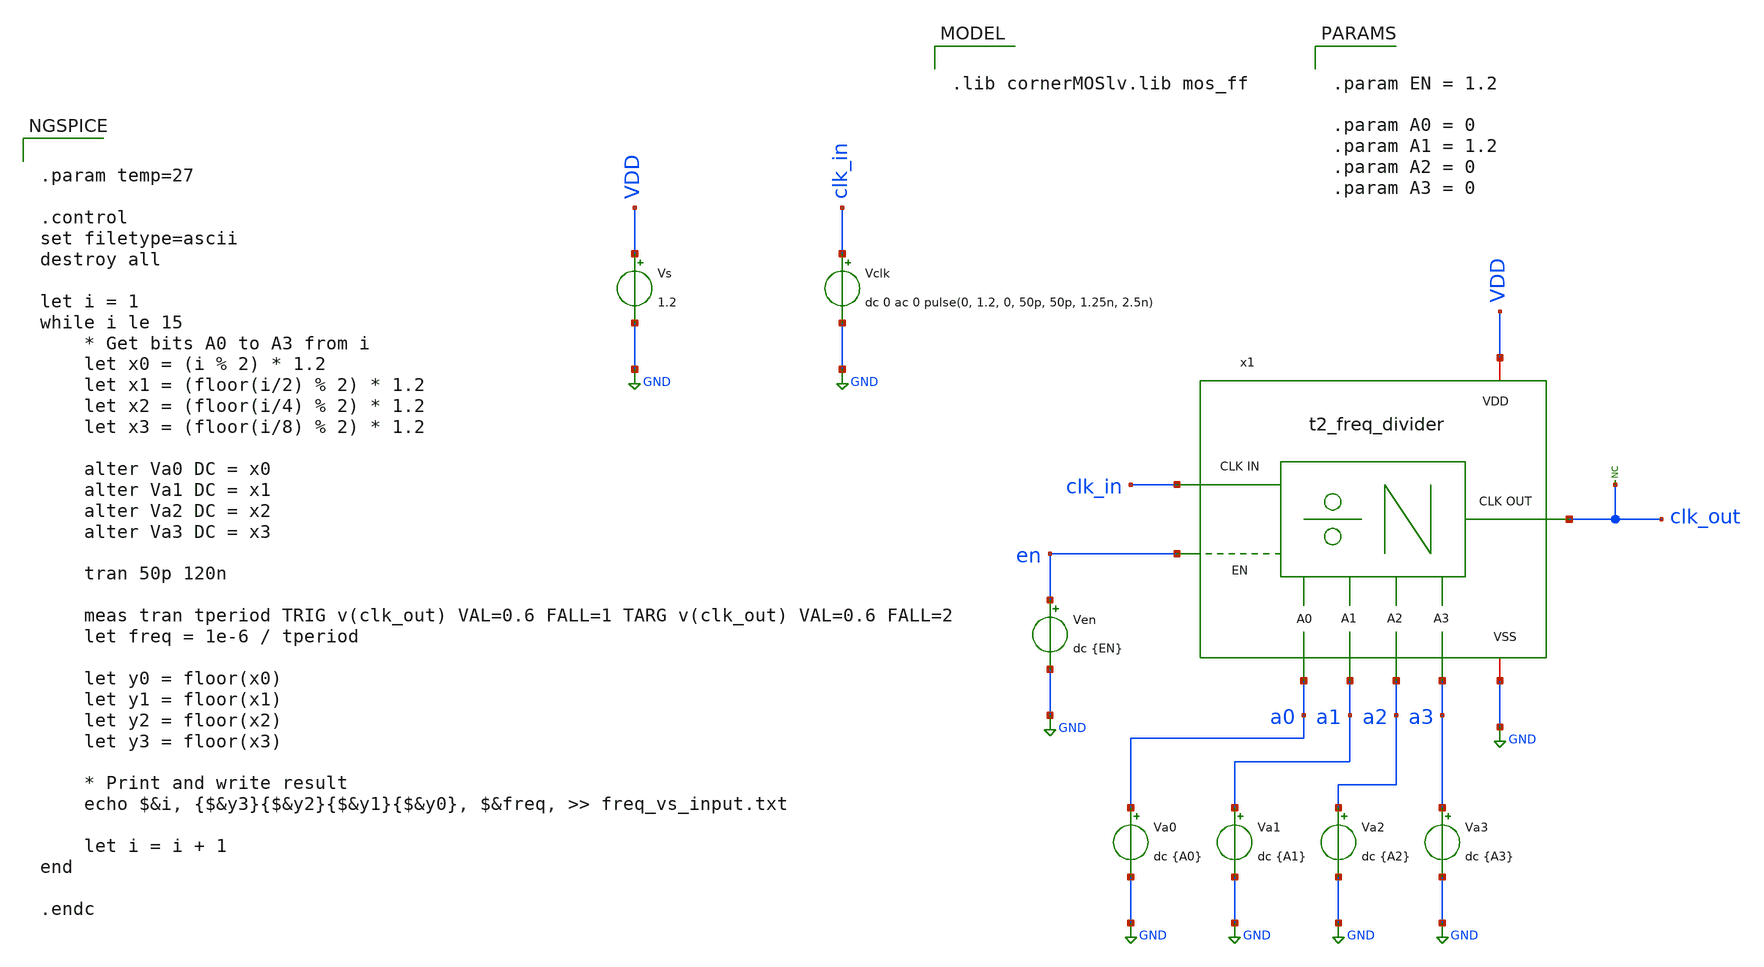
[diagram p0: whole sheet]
** sch_path: Team 2 Design/design_data/xschem/t2_freq_divider_sweep.sch
**.subckt t2_freq_divider_sweep
Vs VDD GND 1.2
Vclk clk_in GND dc 0 ac 0 pulse(0, 1.2, 0, 50p, 50p, 1.25n, 2.5n)
x1 VDD GND clk_in en a0 a1 a2 a3 clk_out t2_freq_divider
* noconn clk_out
Ven en GND dc {EN}
Va0 a0 GND dc {A0}
Va1 a1 GND dc {A1}
Va2 a2 GND dc {A2}
Va3 a3 GND dc {A3}
**** begin user architecture code


.param temp=27

.control
set filetype=ascii
destroy all

let i = 1
while i le 15
    * Get bits A0 to A3 from i
    let x0 = (i % 2) * 1.2
    let x1 = (floor(i/2) % 2) * 1.2
    let x2 = (floor(i/4) % 2) * 1.2
    let x3 = (floor(i/8) % 2) * 1.2

    alter Va0 DC = x0
    alter Va1 DC = x1
    alter Va2 DC = x2
    alter Va3 DC = x3

    tran 50p 120n

    meas tran tperiod TRIG v(clk_out) VAL=0.6 FALL=1 TARG v(clk_out) VAL=0.6 FALL=2
    let freq = 1e-6 / tperiod

    let y0 = floor(x0)
    let y1 = floor(x1)
    let y2 = floor(x2)
    let y3 = floor(x3)

    * Print and write result
    echo $&i, {$&y3}{$&y2}{$&y1}{$&y0}, $&freq, >> freq_vs_input.txt

    let i = i + 1
end

.endc



.lib cornerMOSlv.lib mos_ff



.param EN = 1.2

.param A0 = 0
.param A1 = 1.2
.param A2 = 0
.param A3 = 0


**** end user architecture code
**.ends
.GLOBAL GND
.end
